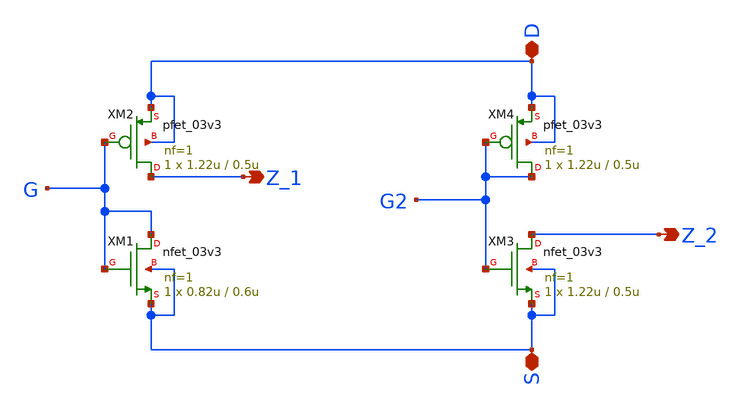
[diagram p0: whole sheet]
** sch_path: integration/tieH_L.sch
**.subckt tieH_L Z_1 D S Z_2
*.opin Z_1
*.iopin D
*.iopin S
*.opin Z_2
XM1 G G S S nfet_03v3 L=0.6u W=0.82u nf=1 ad='int((nf+1)/2) * W/nf * 0.18u' as='int((nf+2)/2) * W/nf * 0.18u'
+ pd='2*int((nf+1)/2) * (W/nf + 0.18u)' ps='2*int((nf+2)/2) * (W/nf + 0.18u)' nrd='0.18u / W' nrs='0.18u / W'
+ sa=0 sb=0 sd=0 m=1
XM2 Z_1 G D D pfet_03v3 L=0.5u W=1.22u nf=1 ad='int((nf+1)/2) * W/nf * 0.18u' as='int((nf+2)/2) * W/nf * 0.18u'
+ pd='2*int((nf+1)/2) * (W/nf + 0.18u)' ps='2*int((nf+2)/2) * (W/nf + 0.18u)' nrd='0.18u / W' nrs='0.18u / W'
+ sa=0 sb=0 sd=0 m=1
XM3 Z_2 G2 S S nfet_03v3 L=0.5u W=1.22u nf=1 ad='int((nf+1)/2) * W/nf * 0.18u' as='int((nf+2)/2) * W/nf * 0.18u'
+ pd='2*int((nf+1)/2) * (W/nf + 0.18u)' ps='2*int((nf+2)/2) * (W/nf + 0.18u)' nrd='0.18u / W' nrs='0.18u / W'
+ sa=0 sb=0 sd=0 m=1
XM4 G2 G2 D D pfet_03v3 L=0.5u W=1.22u nf=1 ad='int((nf+1)/2) * W/nf * 0.18u' as='int((nf+2)/2) * W/nf * 0.18u'
+ pd='2*int((nf+1)/2) * (W/nf + 0.18u)' ps='2*int((nf+2)/2) * (W/nf + 0.18u)' nrd='0.18u / W' nrs='0.18u / W'
+ sa=0 sb=0 sd=0 m=1
**.ends
.end
